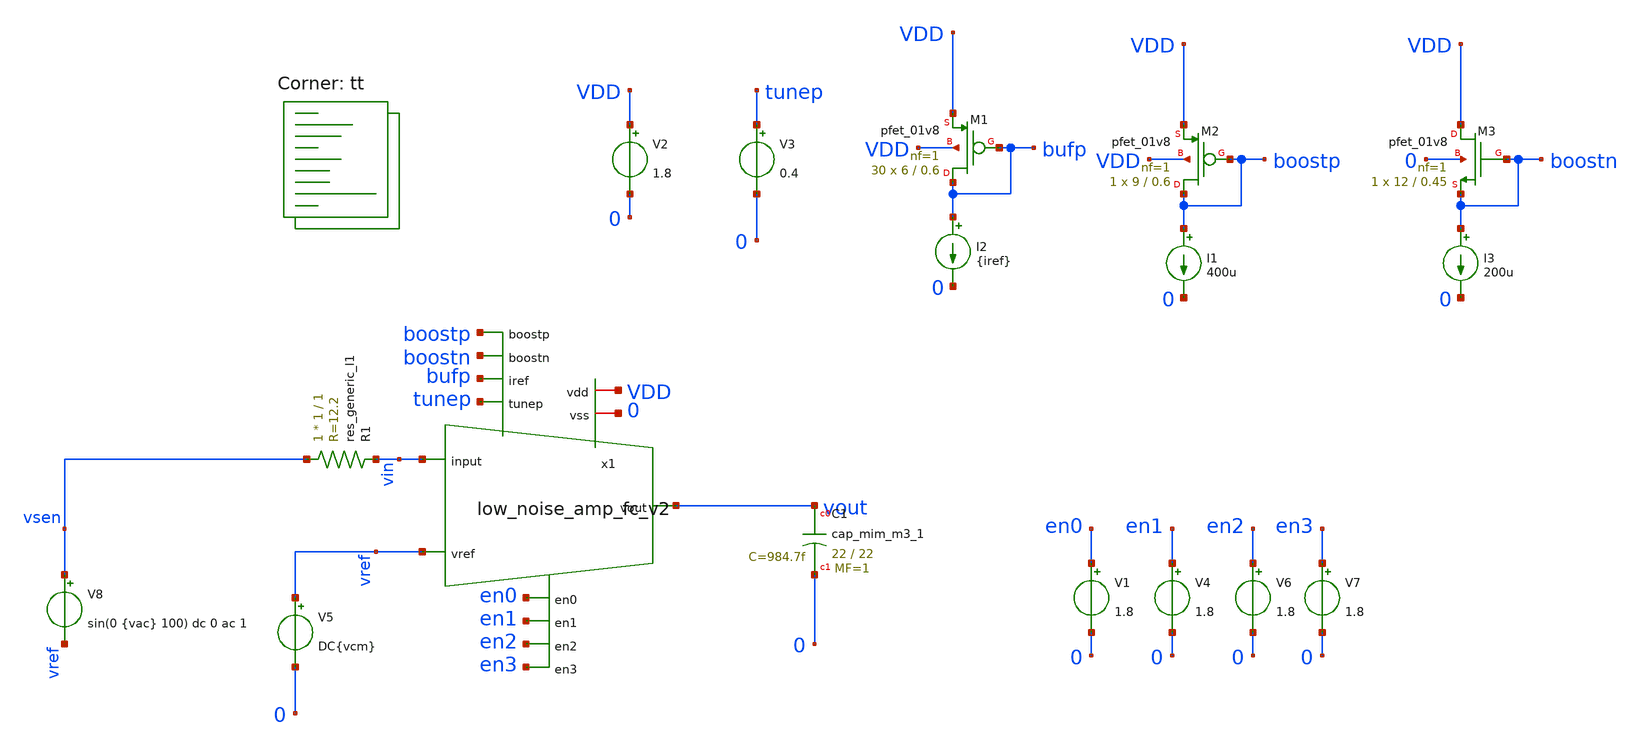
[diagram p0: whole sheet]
** sch_path: design/xschem/low_noise_amp_fc_v1_loopgain_tb.sch
**.subckt low_noise_amp_fc_v1_loopgain_tb
V2 VDD 0 1.8
V5 vref 0 DC{vcm}
XC1 vout 0 sky130_fd_pr__cap_mim_m3_1 W=22 L=22 MF=1 m=1
V1 en0 0 1.8
V4 en1 0 1.8
V6 en2 0 1.8
V7 en3 0 1.8
XM1 bufp bufp VDD VDD sky130_fd_pr__pfet_01v8 L=0.6 W=6 nf=1 ad='W * 0.29' as='W * 0.29' pd='2 * (W + 0.29)'
+ ps='2 * (W + 0.29)' nrd='0.29 / W' nrs='0.29 / W' sa=0 sb=0 sd=0 mult=30 m=30
I2 bufp 0 {iref}
V8 vsen vref sin(0 {vac} 100) dc 0 ac 1
R1 vsen vin sky130_fd_pr__res_generic_l1 W=1 L=1 m=1
V3 tunep 0 0.4
XM2 boostp boostp VDD VDD sky130_fd_pr__pfet_01v8 L=0.6 W=9 nf=1 ad='W * 0.29' as='W * 0.29' pd='2 * (W + 0.29)'
+ ps='2 * (W + 0.29)' nrd='0.29 / W' nrs='0.29 / W' sa=0 sb=0 sd=0 mult=1 m=1
I1 boostp 0 400u
x1 en0 en1 en2 tunep en3 VDD bufp vref vout 0 vin boostn boostp low_noise_amp_fc_v2
XM3 VDD boostn boostn 0 sky130_fd_pr__pfet_01v8 L=0.45 W=12 nf=1 ad='W * 0.29' as='W * 0.29' pd='2 * (W + 0.29)'
+ ps='2 * (W + 0.29)' nrd='0.29 / W' nrs='0.29 / W' sa=0 sb=0 sd=0 mult=1 m=1
I3 boostn 0 200u
**** begin user architecture code
.lib $::SKYWATER_MODELS/sky130.lib.spice tt



* ngspice commands



* Circuit Parameters
*.param iref1 = 200u
.param iref = 200u
.param vdd  = 1.8
.param vss  = 0.0
.param vcm  = 0.8
.param vac  = 5u
.options TEMP = 35.0


* OP Parameters & Singals to save
.save all
  @M.X1.XM2.msky130_fd_pr__pfet_01v8[id] @M.X1.XM2.msky130_fd_pr__pfet_01v8[vth]
+ @M.X1.XM2.msky130_fd_pr__pfet_01v8[vgs] @M.X1.XM2.msky130_fd_pr__pfet_01v8[vds] @M.X1.XM2.msky130_fd_pr__pfet_01v8[vdsat]
+ @M.X1.XM2.msky130_fd_pr__pfet_01v8[gm] @M.X1.XM2.msky130_fd_pr__pfet_01v8[gds]  @M.X1.XM1.msky130_fd_pr__pfet_01v8[id]
+ @M.X1.XM1.msky130_fd_pr__pfet_01v8[vth] @M.X1.XM1.msky130_fd_pr__pfet_01v8[vgs] @M.X1.XM1.msky130_fd_pr__pfet_01v8[vds]
+ @M.X1.XM1.msky130_fd_pr__pfet_01v8[vdsat] @M.X1.XM1.msky130_fd_pr__pfet_01v8[gm] @M.X1.XM1.msky130_fd_pr__pfet_01v8[gds]
+  @M.X1.XM11.msky130_fd_pr__pfet_01v8[id] @M.X1.XM11.msky130_fd_pr__pfet_01v8[vth] @M.X1.XM11.msky130_fd_pr__pfet_01v8[vgs]
+ @M.X1.XM11.msky130_fd_pr__pfet_01v8[vds] @M.X1.XM11.msky130_fd_pr__pfet_01v8[vdsat] @M.X1.XM11.msky130_fd_pr__pfet_01v8[gm]
+ @M.X1.XM11.msky130_fd_pr__pfet_01v8[gds]  @M.X1.XM7.msky130_fd_pr__pfet_01v8[id] @M.X1.XM7.msky130_fd_pr__pfet_01v8[vth]
+ @M.X1.XM7.msky130_fd_pr__pfet_01v8[vgs] @M.X1.XM7.msky130_fd_pr__pfet_01v8[vds] @M.X1.XM7.msky130_fd_pr__pfet_01v8[vdsat]
+ @M.X1.XM7.msky130_fd_pr__pfet_01v8[gm] @M.X1.XM7.msky130_fd_pr__pfet_01v8[gds]  @M.X1.XM9.msky130_fd_pr__nfet_01v8[id]
+ @M.X1.XM9.msky130_fd_pr__nfet_01v8[vth] @M.X1.XM9.msky130_fd_pr__nfet_01v8[vgs] @M.X1.XM9.msky130_fd_pr__nfet_01v8[vds]
+ @M.X1.XM9.msky130_fd_pr__nfet_01v8[vdsat] @M.X1.XM9.msky130_fd_pr__nfet_01v8[gm] @M.X1.XM9.msky130_fd_pr__nfet_01v8[gds]
+  @M.X1.XM10.msky130_fd_pr__nfet_01v8[id] @M.X1.XM10.msky130_fd_pr__nfet_01v8[vth] @M.X1.XM10.msky130_fd_pr__nfet_01v8[vgs]
+ @M.X1.XM10.msky130_fd_pr__nfet_01v8[vds] @M.X1.XM10.msky130_fd_pr__nfet_01v8[vdsat] @M.X1.XM10.msky130_fd_pr__nfet_01v8[gm]
+ @M.X1.XM10.msky130_fd_pr__nfet_01v8[gds]  @M.X1.XM12.msky130_fd_pr__pfet_01v8[id] @M.X1.XM12.msky130_fd_pr__pfet_01v8[vth]
+ @M.X1.XM12.msky130_fd_pr__pfet_01v8[vgs] @M.X1.XM12.msky130_fd_pr__pfet_01v8[vds] @M.X1.XM12.msky130_fd_pr__pfet_01v8[vdsat]
+ @M.X1.XM12.msky130_fd_pr__pfet_01v8[gm] @M.X1.XM12.msky130_fd_pr__pfet_01v8[gds]  @M.X1.XM16.msky130_fd_pr__nfet_01v8[id]
+ @M.X1.XM16.msky130_fd_pr__nfet_01v8[vth] @M.X1.XM16.msky130_fd_pr__nfet_01v8[vgs] @M.X1.XM16.msky130_fd_pr__nfet_01v8[vds]
+ @M.X1.XM16.msky130_fd_pr__nfet_01v8[vdsat] @M.X1.XM16.msky130_fd_pr__nfet_01v8[gm] @M.X1.XM16.msky130_fd_pr__nfet_01v8[gds]
+  @M.X1.XM12.msky130_fd_pr__pfet_01v8[id] @M.X1.XM12.msky130_fd_pr__pfet_01v8[vth] @M.X1.XM12.msky130_fd_pr__pfet_01v8[vgs]
+ @M.X1.XM12.msky130_fd_pr__pfet_01v8[vds] @M.X1.XM12.msky130_fd_pr__pfet_01v8[vdsat] @M.X1.XM12.msky130_fd_pr__pfet_01v8[gm]
+ @M.X1.XM12.msky130_fd_pr__pfet_01v8[gds] @M.X1.XM12.msky130_fd_pr__pfet_01v8[gdm]  @M.X1.XM8.msky130_fd_pr__pfet_01v8[id]
+ @M.X1.XM8.msky130_fd_pr__pfet_01v8[vth] @M.X1.XM8.msky130_fd_pr__pfet_01v8[vgs] @M.X1.XM8.msky130_fd_pr__pfet_01v8[vds]
+ @M.X1.XM8.msky130_fd_pr__pfet_01v8[vdsat] @M.X1.XM8.msky130_fd_pr__pfet_01v8[gm] @M.X1.XM8.msky130_fd_pr__pfet_01v8[gds]
+  @M.X1.XM15.msky130_fd_pr__pfet_01v8[id] @M.X1.XM15.msky130_fd_pr__pfet_01v8[vth] @M.X1.XM15.msky130_fd_pr__pfet_01v8[vgs]
+ @M.X1.XM15.msky130_fd_pr__pfet_01v8[vds] @M.X1.XM15.msky130_fd_pr__pfet_01v8[vdsat] @M.X1.XM15.msky130_fd_pr__pfet_01v8[gm]
+ @M.X1.XM15.msky130_fd_pr__pfet_01v8[gds] @M.X1.XM15.msky130_fd_pr__pfet_01v8[gdm]


*Simulations
.control
  ac dec 200 0.001 1G
  setplot ac1
  meas ac GBW when vdb(vout)=0
  meas ac DCG find vdb(vout) at=10
  meas ac PM find vp(vout) when vdb(vout)=0
  print PM*180/PI
  meas ac GM find vdb(vout) when vp(vout)=0
  plot vdb(vout) {vp(vout)*180/PI}
  write opamp_closeloop_ac1_v1.raw

  reset
  tran 1u 20m
  setplot tran1
  plot v(vsen) v(vout)
  write opamp_closeloop_tran1.raw

  reset
  noise v(vout) V8 dec 200 0.001 1G 1
  setplot noise1
  plot inoise_spectrum onoise_spectrum
  *print inoise_spectrum
  *print onoise_spectrum
  setplot noise2
  *plot inoise_total onoise_total
  print inoise_total
  print onoise_total
  write opamp_closeloop_noise_v1.raw

  reset
  op
  setplot op1
  print vout
  write opamp_closeloop_op1_v1_fctoday.raw

.endc

.end



**** end user architecture code
**.ends

* expanding   symbol:  low_noise_amp_fc_v2.sym # of pins=13
** sym_path: design/xschem/low_noise_amp_fc_v2.sym
** sch_path: design/xschem/low_noise_amp_fc_v2.sch
.subckt low_noise_amp_fc_v2 en0 en1 en2 tunep en3 vdd iref vref vout vss input boostn boostp
*.iopin vdd
*.iopin vss
*.ipin vref
*.opin vout
*.ipin iref
*.ipin en0
*.ipin en1
*.ipin en2
*.ipin en3
*.ipin input
*.ipin tunep
*.ipin boostp
*.ipin boostn
XM1 vbn vin vp vdd sky130_fd_pr__pfet_01v8 L=0.3 W=3 nf=1 ad='W * 0.29' as='W * 0.29' pd='2 * (W + 0.29)'
+ ps='2 * (W + 0.29)' nrd='0.29 / W' nrs='0.29 / W' sa=0 sb=0 sd=0 mult=400 m=400
XM2 voe1 vref vp vdd sky130_fd_pr__pfet_01v8 L=0.3 W=3 nf=1 ad='W * 0.29' as='W * 0.29' pd='2 * (W + 0.29)'
+ ps='2 * (W + 0.29)' nrd='0.29 / W' nrs='0.29 / W' sa=0 sb=0 sd=0 mult=400 m=400
XM3 vbn vbn vss vss sky130_fd_pr__nfet_01v8 L=0.3 W=3 nf=1 ad='W * 0.29' as='W * 0.29' pd='2 * (W + 0.29)'
+ ps='2 * (W + 0.29)' nrd='0.29 / W' nrs='0.29 / W' sa=0 sb=0 sd=0 mult=30 m=30
XM4 voe1 voe1 vss vss sky130_fd_pr__nfet_01v8 L=0.3 W=3 nf=1 ad='W * 0.29' as='W * 0.29' pd='2 * (W + 0.29)'
+ ps='2 * (W + 0.29)' nrd='0.29 / W' nrs='0.29 / W' sa=0 sb=0 sd=0 mult=30 m=30
XM5 vp iref vdd vdd sky130_fd_pr__pfet_01v8 L=0.3 W=3 nf=1 ad='W * 0.29' as='W * 0.29' pd='2 * (W + 0.29)'
+ ps='2 * (W + 0.29)' nrd='0.29 / W' nrs='0.29 / W' sa=0 sb=0 sd=0 mult=30 m=30
XM7 net5 vbna vdd vdd sky130_fd_pr__pfet_01v8 L=0.3 W=3 nf=1 ad='W * 0.29' as='W * 0.29' pd='2 * (W + 0.29)'
+ ps='2 * (W + 0.29)' nrd='0.29 / W' nrs='0.29 / W' sa=0 sb=0 sd=0 mult=15 m=15
XM8 vbna vbna vdd vdd sky130_fd_pr__pfet_01v8 L=0.3 W=3 nf=1 ad='W * 0.29' as='W * 0.29' pd='2 * (W + 0.29)'
+ ps='2 * (W + 0.29)' nrd='0.29 / W' nrs='0.29 / W' sa=0 sb=0 sd=0 mult=15 m=15
XM6 net6 voe1 vss vss sky130_fd_pr__nfet_01v8 L=0.45 W=4.5 nf=1 ad='W * 0.29' as='W * 0.29' pd='2 * (W + 0.29)'
+ ps='2 * (W + 0.29)' nrd='0.29 / W' nrs='0.29 / W' sa=0 sb=0 sd=0 mult=150 m=150
XM9 vbna vbn vss vss sky130_fd_pr__nfet_01v8 L=0.3 W=3 nf=1 ad='W * 0.29' as='W * 0.29' pd='2 * (W + 0.29)'
+ ps='2 * (W + 0.29)' nrd='0.29 / W' nrs='0.29 / W' sa=0 sb=0 sd=0 mult=30 m=30
XM28 nen0 en0 vdd vdd sky130_fd_pr__pfet_01v8 L=0.15 W=1.0 nf=1 ad='int((nf+1)/2) * W/nf * 0.29' as='int((nf+2)/2) * W/nf * 0.29'
+ pd='2*int((nf+1)/2) * (W/nf + 0.29)' ps='2*int((nf+2)/2) * (W/nf + 0.29)' nrd='0.29 / W' nrs='0.29 / W'
+ sa=0 sb=0 sd=0 mult=1 m=1
XM29 nen0 en0 vss vss sky130_fd_pr__nfet_01v8 L=0.15 W=0.65 nf=1 ad='int((nf+1)/2) * W/nf * 0.29' as='int((nf+2)/2) * W/nf * 0.29'
+ pd='2*int((nf+1)/2) * (W/nf + 0.29)' ps='2*int((nf+2)/2) * (W/nf + 0.29)' nrd='0.29 / W' nrs='0.29 / W'
+ sa=0 sb=0 sd=0 mult=1 m=1
XM30 nen1 en1 vdd vdd sky130_fd_pr__pfet_01v8 L=0.15 W=1.0 nf=1 ad='int((nf+1)/2) * W/nf * 0.29' as='int((nf+2)/2) * W/nf * 0.29'
+ pd='2*int((nf+1)/2) * (W/nf + 0.29)' ps='2*int((nf+2)/2) * (W/nf + 0.29)' nrd='0.29 / W' nrs='0.29 / W'
+ sa=0 sb=0 sd=0 mult=1 m=1
XM31 nen1 en1 vss vss sky130_fd_pr__nfet_01v8 L=0.15 W=0.65 nf=1 ad='int((nf+1)/2) * W/nf * 0.29' as='int((nf+2)/2) * W/nf * 0.29'
+ pd='2*int((nf+1)/2) * (W/nf + 0.29)' ps='2*int((nf+2)/2) * (W/nf + 0.29)' nrd='0.29 / W' nrs='0.29 / W'
+ sa=0 sb=0 sd=0 mult=1 m=1
XM32 nen2 en2 vdd vdd sky130_fd_pr__pfet_01v8 L=0.15 W=1.0 nf=1 ad='int((nf+1)/2) * W/nf * 0.29' as='int((nf+2)/2) * W/nf * 0.29'
+ pd='2*int((nf+1)/2) * (W/nf + 0.29)' ps='2*int((nf+2)/2) * (W/nf + 0.29)' nrd='0.29 / W' nrs='0.29 / W'
+ sa=0 sb=0 sd=0 mult=1 m=1
XM33 nen2 en2 vss vss sky130_fd_pr__nfet_01v8 L=0.15 W=0.65 nf=1 ad='int((nf+1)/2) * W/nf * 0.29' as='int((nf+2)/2) * W/nf * 0.29'
+ pd='2*int((nf+1)/2) * (W/nf + 0.29)' ps='2*int((nf+2)/2) * (W/nf + 0.29)' nrd='0.29 / W' nrs='0.29 / W'
+ sa=0 sb=0 sd=0 mult=1 m=1
XM34 nen3 en3 vdd vdd sky130_fd_pr__pfet_01v8 L=0.15 W=1.0 nf=1 ad='int((nf+1)/2) * W/nf * 0.29' as='int((nf+2)/2) * W/nf * 0.29'
+ pd='2*int((nf+1)/2) * (W/nf + 0.29)' ps='2*int((nf+2)/2) * (W/nf + 0.29)' nrd='0.29 / W' nrs='0.29 / W'
+ sa=0 sb=0 sd=0 mult=1 m=1
XM35 nen3 en3 vss vss sky130_fd_pr__nfet_01v8 L=0.15 W=0.65 nf=1 ad='int((nf+1)/2) * W/nf * 0.29' as='int((nf+2)/2) * W/nf * 0.29'
+ pd='2*int((nf+1)/2) * (W/nf + 0.29)' ps='2*int((nf+2)/2) * (W/nf + 0.29)' nrd='0.29 / W' nrs='0.29 / W'
+ sa=0 sb=0 sd=0 mult=1 m=1
XC7 vin net4 sky130_fd_pr__cap_mim_m3_1 W=100 L=100 MF=1 m=1
XC8 net1 vin sky130_fd_pr__cap_mim_m3_2 W=100 L=100 MF=1 m=1
XC9 net2 vin sky130_fd_pr__cap_mim_m3_2 W=100 L=100 MF=1 m=1
XC10 vin net3 sky130_fd_pr__cap_mim_m3_1 W=100 L=100 MF=1 m=1
XM13 input en0 net4 vss sky130_fd_pr__nfet_01v8 L=2.0 W=2.0 nf=1 ad='int((nf+1)/2) * W/nf * 0.29' as='int((nf+2)/2) * W/nf * 0.29'
+ pd='2*int((nf+1)/2) * (W/nf + 0.29)' ps='2*int((nf+2)/2) * (W/nf + 0.29)' nrd='0.29 / W' nrs='0.29 / W'
+ sa=0 sb=0 sd=0 mult=1 m=1
XM14 net4 nen0 input vdd sky130_fd_pr__pfet_01v8 L=2.0 W=2.0 nf=1 ad='int((nf+1)/2) * W/nf * 0.29' as='int((nf+2)/2) * W/nf * 0.29'
+ pd='2*int((nf+1)/2) * (W/nf + 0.29)' ps='2*int((nf+2)/2) * (W/nf + 0.29)' nrd='0.29 / W' nrs='0.29 / W'
+ sa=0 sb=0 sd=0 mult=1 m=1
XM18 input en1 net1 vss sky130_fd_pr__nfet_01v8 L=2.0 W=2.0 nf=1 ad='int((nf+1)/2) * W/nf * 0.29' as='int((nf+2)/2) * W/nf * 0.29'
+ pd='2*int((nf+1)/2) * (W/nf + 0.29)' ps='2*int((nf+2)/2) * (W/nf + 0.29)' nrd='0.29 / W' nrs='0.29 / W'
+ sa=0 sb=0 sd=0 mult=1 m=1
XM19 net1 nen1 input vdd sky130_fd_pr__pfet_01v8 L=2.0 W=2.0 nf=1 ad='int((nf+1)/2) * W/nf * 0.29' as='int((nf+2)/2) * W/nf * 0.29'
+ pd='2*int((nf+1)/2) * (W/nf + 0.29)' ps='2*int((nf+2)/2) * (W/nf + 0.29)' nrd='0.29 / W' nrs='0.29 / W'
+ sa=0 sb=0 sd=0 mult=1 m=1
XM20 input en2 net2 vss sky130_fd_pr__nfet_01v8 L=2.0 W=2.0 nf=1 ad='int((nf+1)/2) * W/nf * 0.29' as='int((nf+2)/2) * W/nf * 0.29'
+ pd='2*int((nf+1)/2) * (W/nf + 0.29)' ps='2*int((nf+2)/2) * (W/nf + 0.29)' nrd='0.29 / W' nrs='0.29 / W'
+ sa=0 sb=0 sd=0 mult=1 m=1
XM21 net2 nen2 input vdd sky130_fd_pr__pfet_01v8 L=2.0 W=2.0 nf=1 ad='int((nf+1)/2) * W/nf * 0.29' as='int((nf+2)/2) * W/nf * 0.29'
+ pd='2*int((nf+1)/2) * (W/nf + 0.29)' ps='2*int((nf+2)/2) * (W/nf + 0.29)' nrd='0.29 / W' nrs='0.29 / W'
+ sa=0 sb=0 sd=0 mult=1 m=1
XM22 input en3 net3 vss sky130_fd_pr__nfet_01v8 L=2.0 W=2.0 nf=1 ad='int((nf+1)/2) * W/nf * 0.29' as='int((nf+2)/2) * W/nf * 0.29'
+ pd='2*int((nf+1)/2) * (W/nf + 0.29)' ps='2*int((nf+2)/2) * (W/nf + 0.29)' nrd='0.29 / W' nrs='0.29 / W'
+ sa=0 sb=0 sd=0 mult=1 m=1
XM23 net3 nen3 input vdd sky130_fd_pr__pfet_01v8 L=2.0 W=2.0 nf=1 ad='int((nf+1)/2) * W/nf * 0.29' as='int((nf+2)/2) * W/nf * 0.29'
+ pd='2*int((nf+1)/2) * (W/nf + 0.29)' ps='2*int((nf+2)/2) * (W/nf + 0.29)' nrd='0.29 / W' nrs='0.29 / W'
+ sa=0 sb=0 sd=0 mult=1 m=1
XC6 vout vin sky130_fd_pr__cap_mim_m3_1 W=17 L=17 MF=1 m=1
XM10 vout boostn net6 vss sky130_fd_pr__nfet_01v8 L=0.45 W=12 nf=1 ad='W * 0.29' as='W * 0.29' pd='2 * (W + 0.29)'
+ ps='2 * (W + 0.29)' nrd='0.29 / W' nrs='0.29 / W' sa=0 sb=0 sd=0 mult=1 m=1
XM11 vout boostp net5 vdd sky130_fd_pr__pfet_01v8 L=0.6 W=9 nf=1 ad='W * 0.29' as='W * 0.29' pd='2 * (W + 0.29)'
+ ps='2 * (W + 0.29)' nrd='0.29 / W' nrs='0.29 / W' sa=0 sb=0 sd=0 mult=1 m=1
XM12 vres tunep vin vin sky130_fd_pr__pfet_01v8_hvt L=0.5 W=1 nf=1 ad='int((nf+1)/2) * W/nf * 0.29' as='int((nf+2)/2) * W/nf * 0.29'
+ pd='2*int((nf+1)/2) * (W/nf + 0.29)' ps='2*int((nf+2)/2) * (W/nf + 0.29)' nrd='0.29 / W' nrs='0.29 / W'
+ sa=0 sb=0 sd=0 mult=1 m=1
XM15 vres tunep vout vout sky130_fd_pr__pfet_01v8_hvt L=0.5 W=1 nf=1 ad='int((nf+1)/2) * W/nf * 0.29'
+ as='int((nf+2)/2) * W/nf * 0.29' pd='2*int((nf+1)/2) * (W/nf + 0.29)' ps='2*int((nf+2)/2) * (W/nf + 0.29)'
+ nrd='0.29 / W' nrs='0.29 / W' sa=0 sb=0 sd=0 mult=1 m=1
.ends

.end
